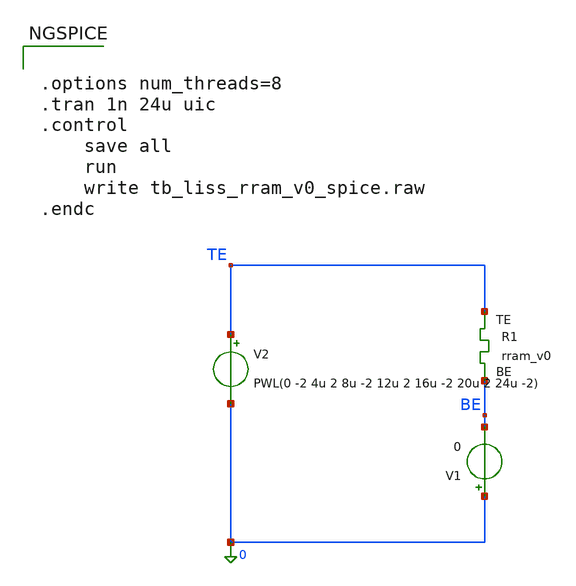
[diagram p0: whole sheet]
** sch_path: memristor_models/wellposed_spice/tb_liss_rram_v0_spice.sch
**.subckt tb_liss_rram_v0_spice
XR1 TE BE rram_v0
V2 TE 0 PWL(0 -2 4u 2 8u -2 12u 2 16u -2 20u 2 24u -2)
V1 0 BE 0
**** begin user architecture code


.options num_threads=8
.tran 1n 24u uic
.control
	save all
	run
	write tb_liss_rram_v0_spice.raw
.endc




** opencircuitdesign pdks install
.inc /home/alex/Desktop/EDA/SNN_IPN/memristor_models/wellposed_spice/wllpsd.spice

**** end user architecture code
**.ends
.end
